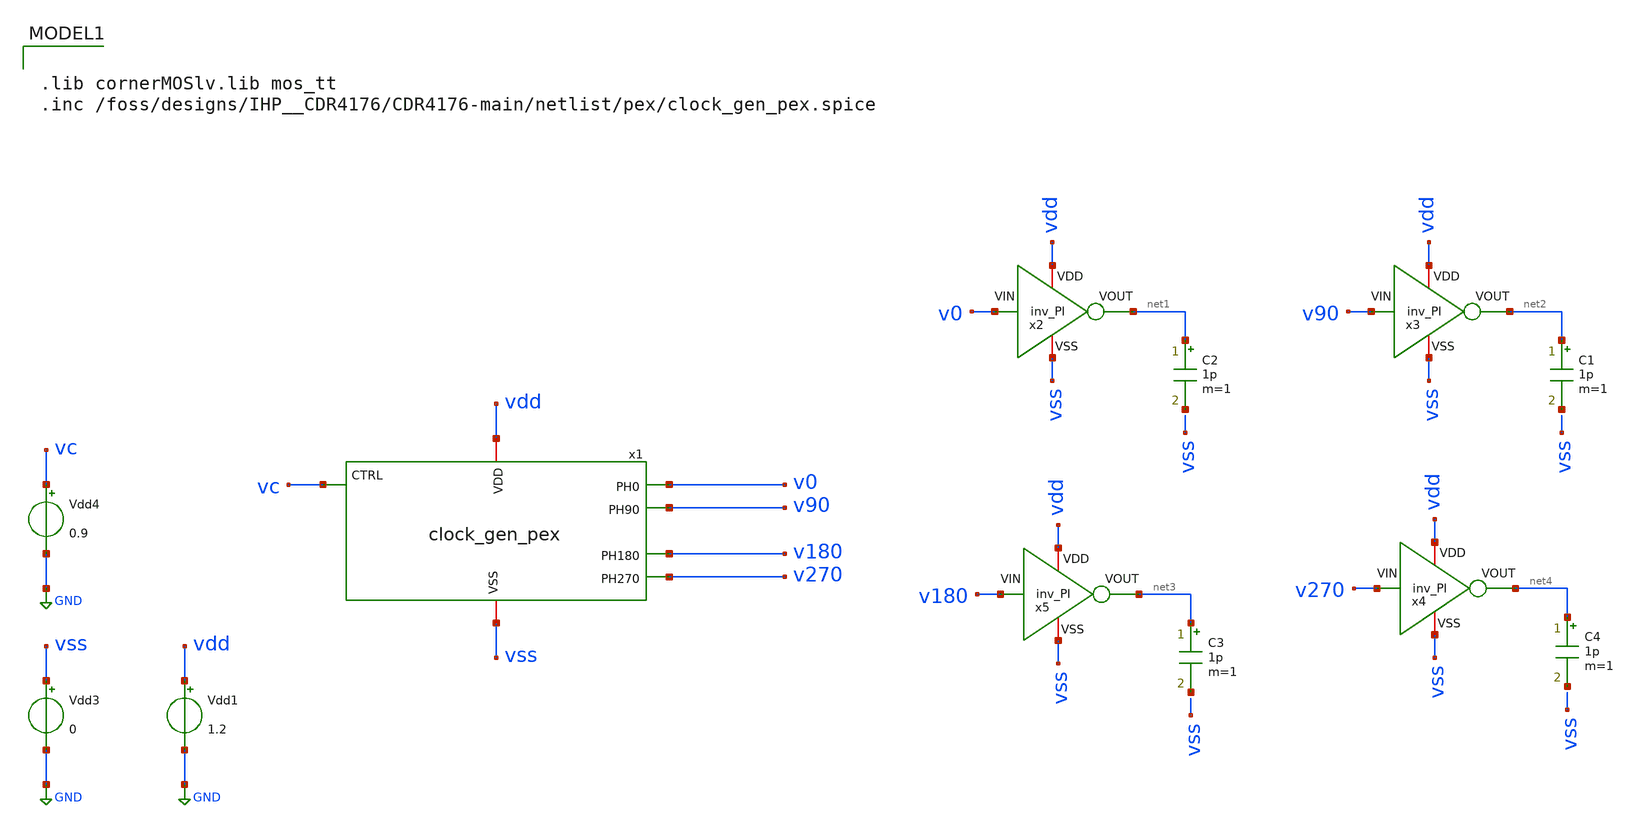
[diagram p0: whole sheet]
** sch_path: CDR4176-main/testbenches/tran/xschem/tb_clock_gen_pex.sch
**.subckt tb_clock_gen_pex
Vdd4 vc GND 0.9
Vdd3 vss GND 0
Vdd1 vdd GND 1.2
C2 net1 net5 1p m=1
C1 net2 net6 1p m=1
C3 net3 net7 1p m=1
C4 net4 net8 1p m=1
x1 v0 v90 vdd vc v180 vss v270 clock_gen_pex
x2 vdd net1 v0 vss inv_PI
x3 vdd net2 v90 vss inv_PI
x4 vdd net4 v270 vss inv_PI
x5 vdd net3 v180 vss inv_PI
**** begin user architecture code

.lib cornerMOSlv.lib mos_tt
.inc /foss/designs/IHP__CDR4176/CDR4176-main/netlist/pex/clock_gen_pex.spice




.options rshunt = 1e9
.options method=gear reltol=5e-3 abstol=1e-8 vntol=1e-4
.save v(v0) v(v90) v(v180) v(v270)



.control
	set ngdebug
	set verbose
	tran 5p 29n

set color0=white
write rosc.raw


*meas tran SKEW0_1 TRIG v(v0) VAL=0.6 RISE=3 TARG v(v1) VAL=0.6 RISE=4
*meas tran SKEW1_2 TRIG v(v1) VAL=0.6 RISE=3 TARG v(v2) VAL=0.6 RISE=4
*meas tran SKEW2_3 TRIG v(v2) VAL=0.6 RISE=3 TARG v(v3) VAL=0.6 RISE=4
*meas tran SKEW3_4 TRIG v(v3) VAL=0.6 RISE=3 TARG v(v4) VAL=0.6 RISE=5
*meas tran SKEW4_5 TRIG v(v4) VAL=0.6 RISE=3 TARG v(v5) VAL=0.6 RISE=4
*meas tran SKEW5_0 TRIG v(v5) VAL=0.6 RISE=3 TARG v(v0) VAL=0.6 RISE=4


*meas tran T0 TRIG v(v0) VAL=0.6 RISE=3 TARG v(v0) VAL=0.6 RISE=4
*meas tran T1 TRIG v(v1) VAL=0.6 RISE=3 TARG v(v1) VAL=0.6 RISE=4
*meas tran T2 TRIG v(v2) VAL=0.6 RISE=3 TARG v(v2) VAL=0.6 RISE=4
*meas tran T3 TRIG v(v3) VAL=0.6 RISE=3 TARG v(v3) VAL=0.6 RISE=4
*meas tran T4 TRIG v(v4) VAL=0.6 RISE=3 TARG v(v4) VAL=0.6 RISE=4
*meas tran T5 TRIG v(v5) VAL=0.6 RISE=3 TARG v(v5) VAL=0.6 RISE=4

*let period_0 = T0
*let period_1 = T1
*let period_2 = T2
*let period_3 = T3
*let period_4 = T4
*let period_5 = T5

*let phase0_1 = ((SKEW0_1 / period_0) * 360) -360
*let phase1_2 = ((SKEW1_2 / period_0) * 360) -360
*let phase2_3 = ((SKEW2_3 / period_0) * 360) -360
*let phase3_4 = ((SKEW3_4 / period_0) * 360) -360
*let phase4_5 = ((SKEW4_5 / period_0) * 360) -360
*let phase5_0 = ((SKEW5_0 / period_0) * 360) -360

*let freq0 = 1/T0
*let freq5 = 1/T5

*meas tran PW0 TRIG v(v0) VAL=0.6 RISE=3 TARG v(v0) VAL=0.6 FALL=4
*meas tran PW1 TRIG v(v1) VAL=0.6 RISE=3 TARG v(v1) VAL=0.6 FALL=4
*meas tran PW2 TRIG v(v2) VAL=0.6 RISE=3 TARG v(v2) VAL=0.6 FALL=4
*meas tran PW3 TRIG v(v3) VAL=0.6 RISE=3 TARG v(v3) VAL=0.6 FALL=4
*meas tran PW4 TRIG v(v4) VAL=0.6 RISE=3 TARG v(v4) VAL=0.6 FALL=4
*meas tran PW5 TRIG v(v5) VAL=0.6 RISE=3 TARG v(v5) VAL=0.6 FALL=4

*let Duty0 = PW0 / period_0
*let Duty1 = PW1 / period_1
*let Duty2 = PW2 / period_2
*let Duty3 = PW3 / period_3
*let Duty4 = PW4 / period_4
*let Duty5 = PW5 / period_5

meas tran SKEW0_90 TRIG v(v0) VAL=0.6 RISE=3 TARG v(v90) VAL=0.6 RISE=3
meas tran SKEW90_180 TRIG v(v90) VAL=0.6 RISE=3 TARG v(v180) VAL=0.6 RISE=4
meas tran SKEW180_270 TRIG v(v180) VAL=0.6 RISE=3 TARG v(v270) VAL=0.6 RISE=3
meas tran SKEW270_0 TRIG v(v270) VAL=0.6 RISE=3 TARG v(v0) VAL=0.6 RISE=3

meas tran T0 TRIG v(v0) VAL=0.6 RISE=3 TARG v(v0) VAL=0.6 RISE=4
meas tran T90 TRIG v(v90) VAL=0.6 RISE=3 TARG v(v90) VAL=0.6 RISE=4
meas tran T180 TRIG v(v180) VAL=0.6 RISE=3 TARG v(v180) VAL=0.6 RISE=4
meas tran T270 TRIG v(v270) VAL=0.6 RISE=3 TARG v(v270) VAL=0.6 RISE=4

let period_0 = T0
let period_90 = T90
let period_180 = T180
let period_270 = T270

let phase0_90 = ((SKEW0_90 / period_0) * 360)
let phase90_180 = ((SKEW90_180 / period_90) * 360)
let phase180_270 = ((SKEW180_270 / period_180) * 360)
let phase270_0 = ((SKEW270_0 / period_270) * 360)

meas tran PW0 TRIG v(v0) VAL=0.6 RISE=4 TARG v(v0) VAL=0.6 FALL=5
meas tran PW90 TRIG v(v90) VAL=0.6 RISE=3 TARG v(v90) VAL=0.6 FALL=4
meas tran PW180 TRIG v(v180) VAL=0.6 RISE=4 TARG v(v180) VAL=0.6 FALL=4
meas tran PW270 TRIG v(v270) VAL=0.6 RISE=4 TARG v(v270) VAL=0.6 FALL=4

let Duty0 = PW0 / period_0
let Duty90 = PW90 / period_90
let Duty180 = PW180 / period_180
let Duty270 = PW270 / period_270

let freq0 = 1/period_0

print phase0_90 phase90_180 phase180_270 phase270_0 Duty0 Duty90 Duty180 Duty270 freq0

.endc


**** end user architecture code
**.ends

* expanding   symbol:  inv_PI/inv_PI.sym # of pins=4
** sym_path: CDR4176-main/schematic/xschem/inv_PI/inv_PI.sym
** sch_path: CDR4176-main/schematic/xschem/inv_PI/inv_PI.sch
.subckt inv_PI VDD VOUT VIN VSS
*.iopin VDD
*.iopin VSS
*.opin VOUT
*.ipin VIN
XM2 VOUT VIN VDD VDD sg13_lv_pmos w=0.45u l=0.13u ng=3 m=1 mm_ok=1
XM1 VOUT VIN VSS VSS sg13_lv_nmos w=0.3u l=0.13u ng=2 m=1 mm_ok=1
.ends

.GLOBAL GND
.end
